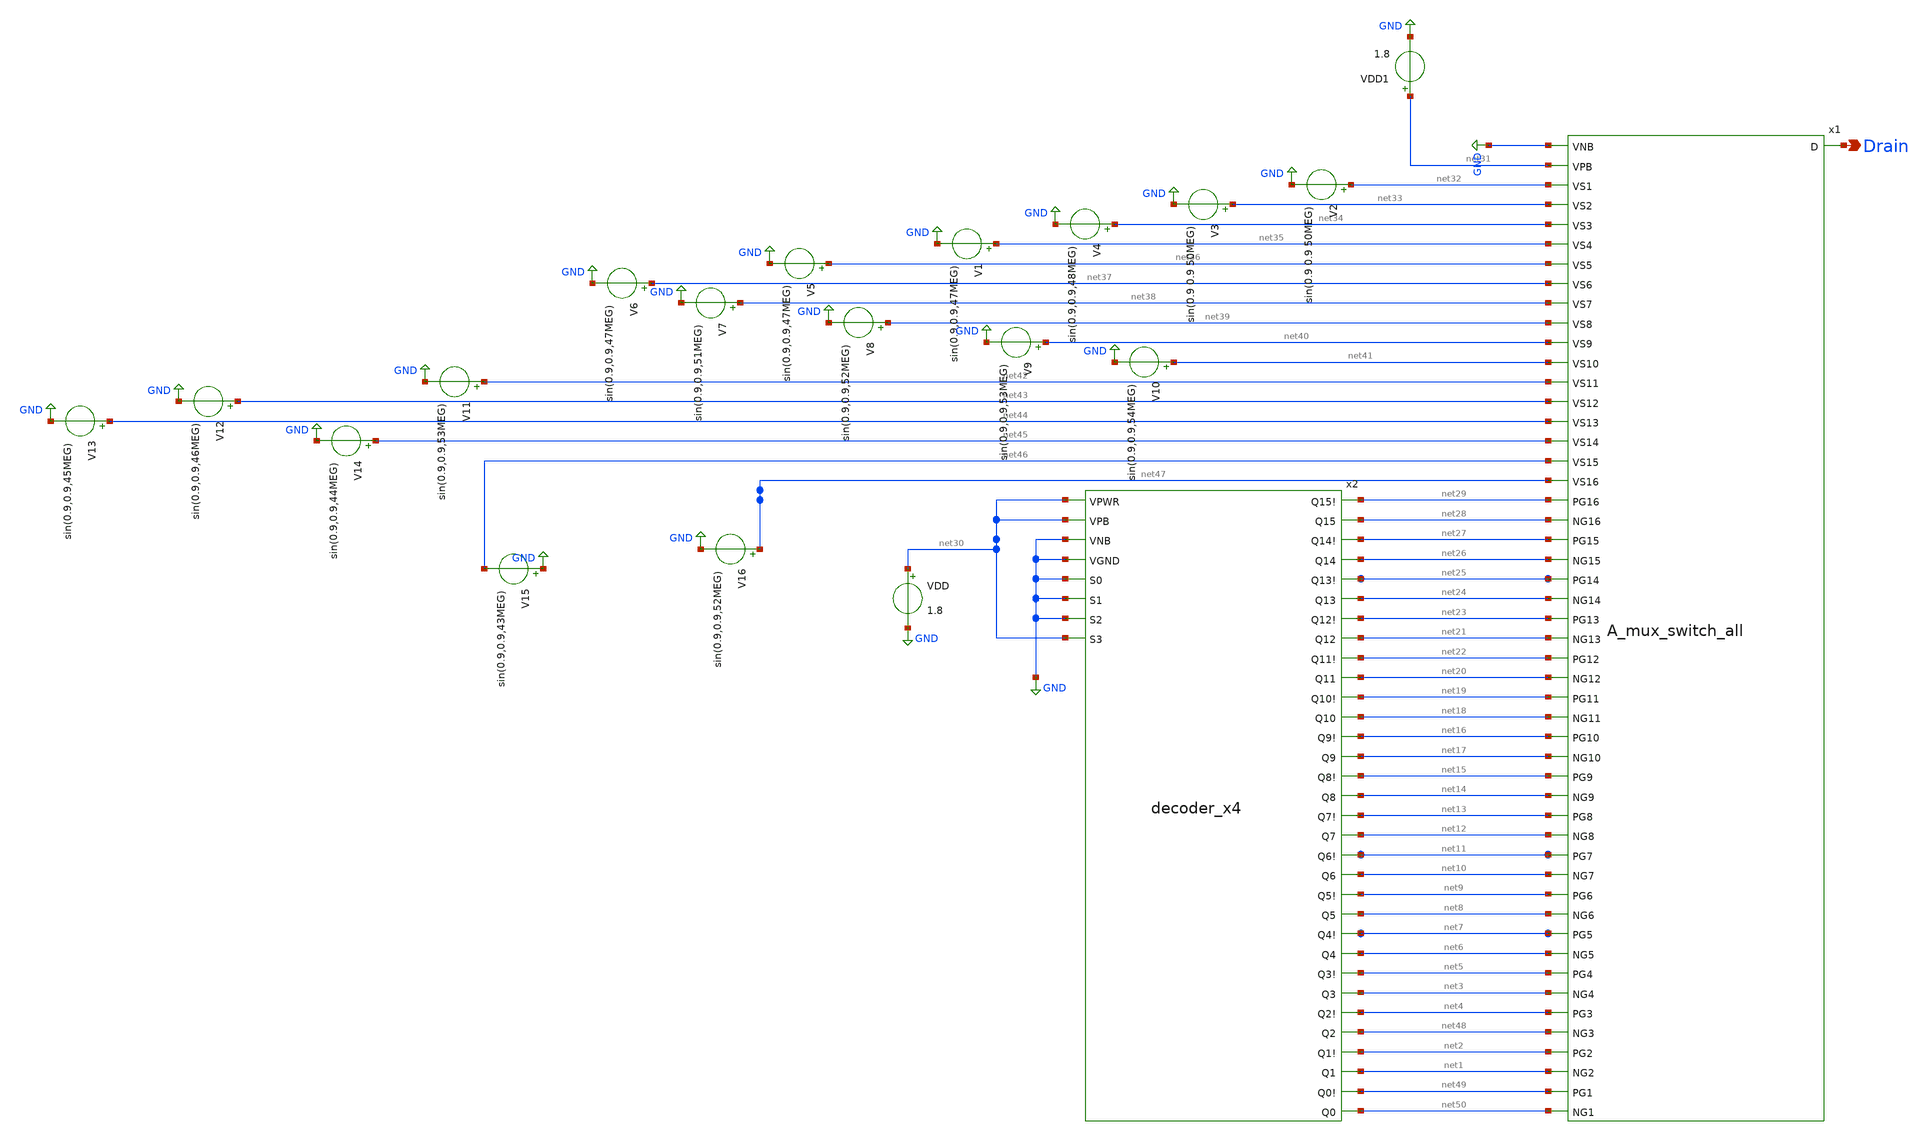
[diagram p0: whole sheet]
** sch_path: compiled 2/decoder_switch.sch
**.subckt decoder_switch Drain
*.opin Drain
x1 GND net31 net32 net50 net49 Drain net33 net1 net2 net34 net48 net4 net35 net3 net5 net36 net6
+ net7 net37 net39 net12 net13 net40 net14 net15 net41 net17 net16 net42 net18 net19 net43 net20 net22
+ net44 net21 net23 net45 net24 net25 net46 net26 net27 net47 net28 net29 net8 net9 net38 net10 net11
+ A_mux_switch_all
x2 net30 net30 GND GND GND GND GND net30 net29 net28 net27 net26 net25 net24 net23 net21 net22 net20
+ net19 net18 net16 net17 net15 net14 net13 net12 net11 net10 net9 net8 net7 net6 net5 net3 net4 net48 net2
+ net1 net49 net50 decoder_x4
VDD net30 GND 1.8
VDD1 net31 GND 1.8
V2 net32 GND sin(0.9 0.9 50MEG)
V1 net35 GND sin(0.9,0.9,47MEG)
V4 net34 GND sin(0.9,0.9,48MEG)
V5 net36 GND sin(0.9,0.9,47MEG)
V6 net37 GND sin(0.9,0.9,47MEG)
V7 net38 GND sin(0.9,0.9,51MEG)
V8 net39 GND sin(0.9,0.9,52MEG)
V9 net40 GND sin(0.9,0.9,53MEG)
V10 net41 GND sin(0.9,0.9,54MEG)
V11 net42 GND sin(0.9,0.9,53MEG)
V12 net43 GND sin(0.9,0.9,46MEG)
V13 net44 GND sin(0.9,0.9,45MEG)
V14 net45 GND sin(0.9,0.9,44MEG)
V15 GND net46 sin(0.9,0.9,43MEG)
V16 net47 GND sin(0.9,0.9,52MEG)
V3 net33 GND sin(0.9 0.9 50MEG)
**** begin user architecture code

** opencircuitdesign pdks install
.lib $::SKYWATER_MODELS/sky130.lib.spice tt
.include $::SKYWATER_STDCELLS/sky130_fd_sc_hd.spice





**** interactive sim
.control
save all
op
tran 1n 1u

write a_mux_switch_test.raw
.endc



**** end user architecture code
**.ends

* expanding   symbol:  A_mux_switch_all.sym # of pins=51
** sym_path: compiled 2/A_mux_switch_all.sym
** sch_path: compiled 2/A_mux_switch_all.sch
.subckt A_mux_switch_all VNB VPB VS1 NG1 PG1 D VS2 NG2 PG2 VS3 NG3 PG3 VS4 NG4 PG4 VS5 NG5 PG5 VS6
+ VS8 NG8 PG8 VS9 NG9 PG9 VS10 NG10 PG10 VS11 NG11 PG11 VS12 NG12 PG12 VS13 NG13 PG13 VS14 NG14 PG14 VS15
+ NG15 PG15 VS16 NG16 PG16 NG6 PG6 VS7 NG7 PG7
*.opin D
*.ipin VS1
*.ipin VS2
*.ipin VS3
*.ipin VS4
*.ipin VS5
*.ipin VS6
*.ipin VS7
*.ipin VS8
*.ipin VS9
*.ipin VS10
*.ipin VS11
*.ipin VS12
*.ipin VS13
*.ipin VS14
*.ipin VS15
*.ipin VS16
*.ipin VPB
*.ipin VNB
*.ipin NG1
*.ipin PG1
*.ipin NG2
*.ipin PG2
*.ipin NG3
*.ipin PG3
*.ipin NG4
*.ipin PG4
*.ipin NG5
*.ipin PG5
*.ipin NG6
*.ipin PG6
*.ipin NG7
*.ipin PG7
*.ipin NG8
*.ipin PG8
*.ipin NG9
*.ipin PG9
*.ipin NG10
*.ipin PG10
*.ipin NG11
*.ipin PG11
*.ipin NG12
*.ipin PG12
*.ipin NG13
*.ipin NG14
*.ipin NG15
*.ipin NG16
*.ipin PG13
*.ipin PG14
*.ipin PG15
*.ipin PG16
x1 VS7 VNB NG7 VPB PG7 D a_mux_switch
x2 VS8 VNB NG8 VPB PG8 D a_mux_switch
x3 VS5 VNB NG5 VPB PG5 D a_mux_switch
x4 VS6 VNB NG6 VPB PG6 D a_mux_switch
x5 VS3 VNB NG3 VPB PG3 D a_mux_switch
x6 VS4 VNB NG4 VPB PG4 D a_mux_switch
x7 VS1 VNB NG1 VPB PG1 D a_mux_switch
x8 VS2 VNB NG2 VPB PG2 D a_mux_switch
x9 VS15 VNB NG15 VPB PG15 D a_mux_switch
x10 VS16 VNB NG16 VPB PG16 D a_mux_switch
x11 VS13 VNB NG13 VPB PG13 D a_mux_switch
x12 VS14 VNB NG14 VPB PG14 D a_mux_switch
x13 VS11 VNB NG11 VPB PG11 D a_mux_switch
x14 VS12 VNB NG12 VPB PG12 D a_mux_switch
x15 VS9 VNB NG9 VPB PG9 D a_mux_switch
x16 VS10 VNB NG10 VPB PG10 D a_mux_switch
.ends


* expanding   symbol:  compiled 2/decoder_x4.sym # of pins=40
** sym_path: compiled 2/decoder_x4.sym
** sch_path: compiled 2/decoder_x4.sch
.subckt decoder_x4 VPWR VPB VNB VGND S0 S1 S2 S3 Q15! Q15 Q14! Q14 Q13! Q13 Q12! Q12 Q11! Q11 Q10!
+ Q10 Q9! Q9 Q8! Q8 Q7! Q7 Q6! Q6 Q5! Q5 Q4! Q4 Q3! Q3 Q2! Q2 Q1! Q1 Q0! Q0
*.ipin S0
*.ipin S1
*.ipin S2
*.ipin S3
*.ipin VGND
*.ipin VPWR
*.ipin VNB
*.ipin VPB
*.opin Q14!
*.opin Q15!
*.opin Q13!
*.opin Q12!
*.opin Q10!
*.opin Q11!
*.opin Q9!
*.opin Q8!
*.opin Q7!
*.opin Q6!
*.opin Q4!
*.opin Q3!
*.opin Q2!
*.opin Q1!
*.opin Q0!
*.opin Q5!
*.opin Q14
*.opin Q15
*.opin Q13
*.opin Q12
*.opin Q10
*.opin Q11
*.opin Q9
*.opin Q8
*.opin Q7
*.opin Q6
*.opin Q4
*.opin Q3
*.opin Q2
*.opin Q1
*.opin Q0
*.opin Q5
x1 S0 S1 S2 S3 VGND VNB VPB VPWR Q15! sky130_fd_sc_hd__nand4_2
x2 S0 S1 S2 net1 VGND VNB VPB VPWR Q14! sky130_fd_sc_hd__nand4_2
x3 S0 S1 net2 S3 VGND VNB VPB VPWR Q13! sky130_fd_sc_hd__nand4_2
x4 S0 S1 net2 net1 VGND VNB VPB VPWR Q12! sky130_fd_sc_hd__nand4_2
x5 S0 net3 S2 S3 VGND VNB VPB VPWR Q11! sky130_fd_sc_hd__nand4_2
x6 S0 net3 S2 net1 VGND VNB VPB VPWR Q10! sky130_fd_sc_hd__nand4_2
x7 S0 net3 net2 S3 VGND VNB VPB VPWR Q9! sky130_fd_sc_hd__nand4_2
x8 S0 net3 net2 net1 VGND VNB VPB VPWR Q8! sky130_fd_sc_hd__nand4_2
x9 net4 S1 S2 S3 VGND VNB VPB VPWR Q7! sky130_fd_sc_hd__nand4_2
x10 net4 S1 S2 net1 VGND VNB VPB VPWR Q6! sky130_fd_sc_hd__nand4_2
x11 net4 S1 net2 S3 VGND VNB VPB VPWR Q5! sky130_fd_sc_hd__nand4_2
x12 net4 S1 net2 net1 VGND VNB VPB VPWR Q4! sky130_fd_sc_hd__nand4_2
x13 net4 net3 S2 S3 VGND VNB VPB VPWR Q3! sky130_fd_sc_hd__nand4_2
x14 net4 net3 S2 net1 VGND VNB VPB VPWR Q2! sky130_fd_sc_hd__nand4_2
x15 net4 net3 net2 S3 VGND VNB VPB VPWR Q1! sky130_fd_sc_hd__nand4_2
x16 net4 net3 net2 net1 VGND VNB VPB VPWR Q0! sky130_fd_sc_hd__nand4_2
x17 S0 VGND VNB VPB VPWR net4 sky130_fd_sc_hd__inv_8
x18 S1 VGND VNB VPB VPWR net3 sky130_fd_sc_hd__inv_8
x19 S2 VGND VNB VPB VPWR net2 sky130_fd_sc_hd__inv_8
x20 S3 VGND VNB VPB VPWR net1 sky130_fd_sc_hd__inv_8
x21 Q15! VGND VNB VPB VPWR Q15 sky130_fd_sc_hd__inv_1
x22 Q14! VGND VNB VPB VPWR Q14 sky130_fd_sc_hd__inv_1
x23 Q13! VGND VNB VPB VPWR Q13 sky130_fd_sc_hd__inv_1
x24 Q12! VGND VNB VPB VPWR Q12 sky130_fd_sc_hd__inv_1
x25 Q11! VGND VNB VPB VPWR Q11 sky130_fd_sc_hd__inv_1
x26 Q10! VGND VNB VPB VPWR Q10 sky130_fd_sc_hd__inv_1
x27 Q9! VGND VNB VPB VPWR Q9 sky130_fd_sc_hd__inv_1
x28 Q8! VGND VNB VPB VPWR Q8 sky130_fd_sc_hd__inv_1
x29 Q7! VGND VNB VPB VPWR Q7 sky130_fd_sc_hd__inv_1
x30 Q6! VGND VNB VPB VPWR Q6 sky130_fd_sc_hd__inv_1
x31 Q5! VGND VNB VPB VPWR Q5 sky130_fd_sc_hd__inv_1
x32 Q4! VGND VNB VPB VPWR Q4 sky130_fd_sc_hd__inv_1
x33 Q3! VGND VNB VPB VPWR Q3 sky130_fd_sc_hd__inv_1
x34 Q2! VGND VNB VPB VPWR Q2 sky130_fd_sc_hd__inv_1
x35 Q1! VGND VNB VPB VPWR Q1 sky130_fd_sc_hd__inv_1
x36 Q0! VGND VNB VPB VPWR Q0 sky130_fd_sc_hd__inv_1
.ends


* expanding   symbol:  compiled 2/a_mux_switch.sym # of pins=6
** sym_path: compiled 2/a_mux_switch.sym
** sch_path: compiled 2/a_mux_switch.sch
.subckt a_mux_switch VS VNB NG VPB PG VD
*.ipin PG
*.ipin NG
*.ipin VS
*.opin VD
*.ipin VPB
*.ipin VNB
XM1 VD PG VS VPB sky130_fd_pr__pfet_01v8 L=0.15 W=60 nf=1 ad='int((nf+1)/2) * W/nf * 0.29' as='int((nf+2)/2) * W/nf * 0.29'
+ pd='2*int((nf+1)/2) * (W/nf + 0.29)' ps='2*int((nf+2)/2) * (W/nf + 0.29)' nrd='0.29 / W' nrs='0.29 / W'
+ sa=0 sb=0 sd=0 mult=1 m=1
XM2 VD NG VS VNB sky130_fd_pr__nfet_01v8 L=0.15 W=40 nf=1 ad='int((nf+1)/2) * W/nf * 0.29' as='int((nf+2)/2) * W/nf * 0.29'
+ pd='2*int((nf+1)/2) * (W/nf + 0.29)' ps='2*int((nf+2)/2) * (W/nf + 0.29)' nrd='0.29 / W' nrs='0.29 / W'
+ sa=0 sb=0 sd=0 mult=1 m=1
.ends

.GLOBAL GND
.end
